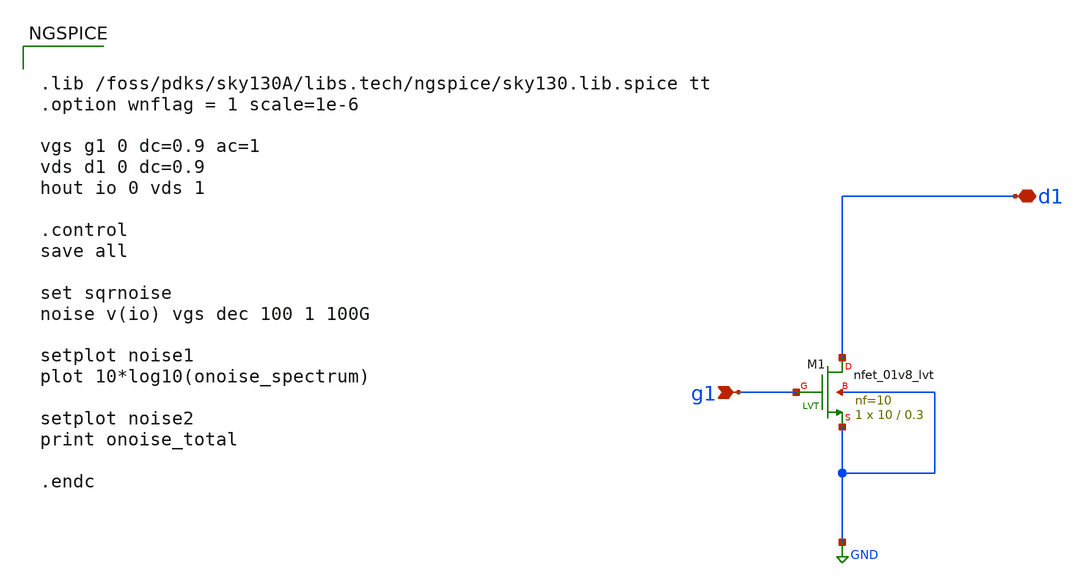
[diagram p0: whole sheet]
** sch_path: mos-noise-corners_jm.sch
**.subckt mos-noise-corners_jm g1 d1
*.ipin g1
*.iopin d1
XM1 d1 g1 GND GND sky130_fd_pr__nfet_01v8_lvt L=0.3 W=10 nf=10 ad='int((nf+1)/2) * W/nf * 0.29' as='int((nf+2)/2) * W/nf * 0.29'
+ pd='2*int((nf+1)/2) * (W/nf + 0.29)' ps='2*int((nf+2)/2) * (W/nf + 0.29)' nrd='0.29 / W' nrs='0.29 / W'
+ sa=0 sb=0 sd=0 mult=1 m=1
**** begin user architecture code


.lib /foss/pdks/sky130A/libs.tech/ngspice/sky130.lib.spice tt
.option wnflag = 1 scale=1e-6

vgs g1 0 dc=0.9 ac=1
vds d1 0 dc=0.9
hout io 0 vds 1

.control
save all

set sqrnoise
noise v(io) vgs dec 100 1 100G

setplot noise1
plot 10*log10(onoise_spectrum)

setplot noise2
print onoise_total

.endc


**** end user architecture code
**.ends
.GLOBAL GND
.end
